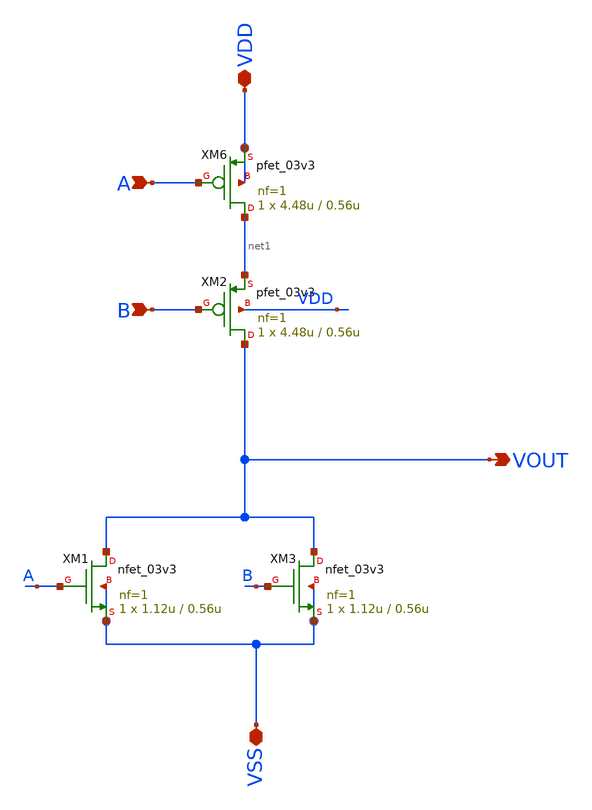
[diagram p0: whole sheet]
** sch_path: PLL-main/schematic/xschem/NOR.sch
**.subckt NOR VSS VDD A B VOUT
*.iopin VSS
*.iopin VDD
*.ipin A
*.ipin B
*.opin VOUT
XM1 VOUT A VSS VSS nfet_03v3 L=0.56u W=1.12u nf=1 ad='int((nf+1)/2) * W/nf * 0.18u' as='int((nf+2)/2) * W/nf * 0.18u'
+ pd='2*int((nf+1)/2) * (W/nf + 0.18u)' ps='2*int((nf+2)/2) * (W/nf + 0.18u)' nrd='0.18u / W' nrs='0.18u / W'
+ sa=0 sb=0 sd=0 m=1
XM2 VOUT B net1 VDD pfet_03v3 L=0.56u W=4.48u nf=1 ad='int((nf+1)/2) * W/nf * 0.18u' as='int((nf+2)/2) * W/nf * 0.18u'
+ pd='2*int((nf+1)/2) * (W/nf + 0.18u)' ps='2*int((nf+2)/2) * (W/nf + 0.18u)' nrd='0.18u / W' nrs='0.18u / W'
+ sa=0 sb=0 sd=0 m=1
XM3 VOUT B VSS VSS nfet_03v3 L=0.56u W=1.12u nf=1 ad='int((nf+1)/2) * W/nf * 0.18u' as='int((nf+2)/2) * W/nf * 0.18u'
+ pd='2*int((nf+1)/2) * (W/nf + 0.18u)' ps='2*int((nf+2)/2) * (W/nf + 0.18u)' nrd='0.18u / W' nrs='0.18u / W'
+ sa=0 sb=0 sd=0 m=1
XM6 net1 A VDD VDD pfet_03v3 L=0.56u W=4.48u nf=1 ad='int((nf+1)/2) * W/nf * 0.18u' as='int((nf+2)/2) * W/nf * 0.18u'
+ pd='2*int((nf+1)/2) * (W/nf + 0.18u)' ps='2*int((nf+2)/2) * (W/nf + 0.18u)' nrd='0.18u / W' nrs='0.18u / W'
+ sa=0 sb=0 sd=0 m=1
**.ends
.end
